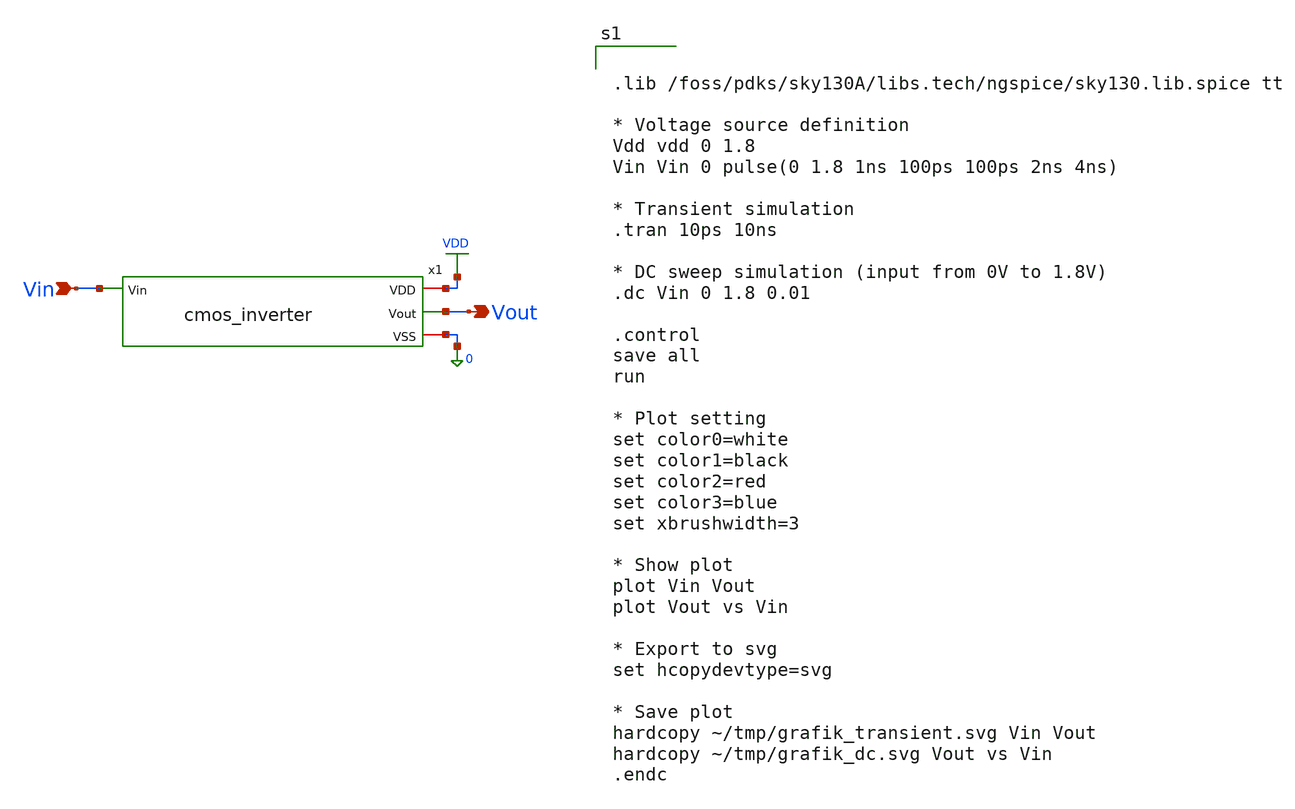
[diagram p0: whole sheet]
** sch_path: cmos_inverter/testbench/inverter_tb.sch
**.subckt inverter_tb Vin Vout
*.ipin Vin
*.opin Vout
x1 VDD Vin Vout 0 cmos_inverter
**** begin user architecture code


.lib /foss/pdks/sky130A/libs.tech/ngspice/sky130.lib.spice tt

* Voltage source definition
Vdd vdd 0 1.8
Vin Vin 0 pulse(0 1.8 1ns 100ps 100ps 2ns 4ns)

* Transient simulation
.tran 10ps 10ns

* DC sweep simulation (input from 0V to 1.8V)
.dc Vin 0 1.8 0.01

.control
save all
run

* Plot setting
set color0=white
set color1=black
set color2=red
set color3=blue
set xbrushwidth=3

* Show plot
plot Vin Vout
plot Vout vs Vin

* Export to svg
set hcopydevtype=svg

* Save plot
hardcopy ~/tmp/grafik_transient.svg Vin Vout
hardcopy ~/tmp/grafik_dc.svg Vout vs Vin
.endc


**** end user architecture code
**.ends

* expanding   symbol:  schematic/cmos_inverter.sym # of pins=4
** sym_path: cmos_inverter/schematic/cmos_inverter.sym
** sch_path: cmos_inverter/schematic/cmos_inverter.sch
.subckt cmos_inverter VDD Vin Vout VSS
*.ipin Vin
*.opin Vout
*.iopin VDD
*.iopin VSS
XM1 Vout Vin VSS VSS sky130_fd_pr__nfet_01v8 L=0.15 W=8 nf=1 ad='int((1 + 1)/2) * 8 / 1 * 0.29' as='int((1 + 2)/2) * 8 / 1 * 0.29'
+ pd='2*int((1 + 1)/2) * (8 / 1 + 0.29)' ps='2*int((1 + 2)/2) * (8 / 1 + 0.29)' nrd='0.29 / 8 ' nrs='0.29 / 8 '
+ sa=0 sb=0 sd=0 mult=1 m=1
XM2 Vout Vin VDD VDD sky130_fd_pr__pfet_01v8 L=0.15 W=24 nf=1 ad='int((1 + 1)/2) * 24 / 1 * 0.29' as='int((1 + 2)/2) * 24 / 1 * 0.29'
+ pd='2*int((1 + 1)/2) * (24 / 1 + 0.29)' ps='2*int((1 + 2)/2) * (24 / 1 + 0.29)' nrd='0.29 / 24 ' nrs='0.29 / 24 '
+ sa=0 sb=0 sd=0 mult=1 m=1
.ends

.GLOBAL VDD
.end
